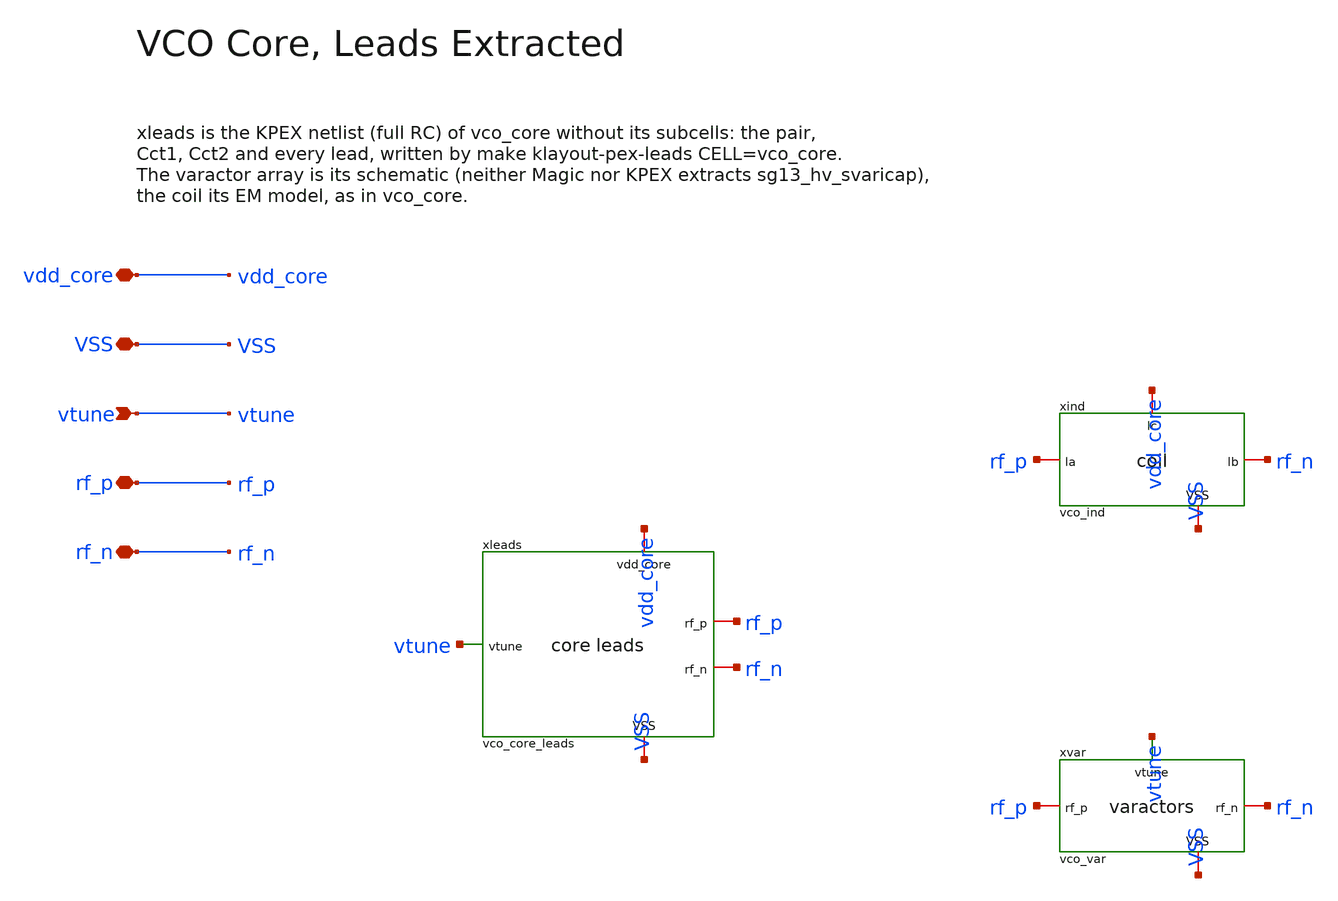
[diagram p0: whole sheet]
** sch_path: macros/vco/testbenches/xschem/vco_core_lpe.sch
**.subckt vco_core_lpe vdd_core VSS vtune rf_p rf_n
*.iopin vdd_core
*.iopin VSS
*.ipin vtune
*.iopin rf_p
*.iopin rf_n
xleads vdd_core VSS vtune rf_p rf_n vco_core_leads
xind rf_p rf_n vdd_core VSS vco_ind
xvar rf_p rf_n vtune VSS vco_var
**.ends

* expanding   symbol:  vco_ind.sym # of pins=4
** sym_path: macros/vco/schematic/xschem/vco_ind.sym
** sch_path: macros/vco/schematic/xschem/vco_ind.sch
.subckt vco_ind la lb lc VSS
*.iopin la
*.iopin lc
*.iopin lb
*.iopin VSS
XL1 la lc lb VSS inductor3 w=4e-6 s=4e-6 d=52e-6 nr_r=2 m=1
x1 la lb lc vco_ind_le
.ends


* expanding   symbol:  vco_var.sym # of pins=4
** sym_path: macros/vco/schematic/xschem/vco_var.sym
** sch_path: macros/vco/schematic/xschem/vco_var.sch
.subckt vco_var rf_p rf_n vtune VSS
*.ipin vtune
*.iopin rf_p
*.iopin rf_n
*.iopin VSS
XCvar1 rf_p vtune rf_n VSS sg13_hv_svaricap w=3.74u l=0.3u Nx=7 mm_ok=1
XCvar2 rf_p vtune rf_n VSS sg13_hv_svaricap w=3.74u l=0.3u Nx=7 mm_ok=1
XCvar3 rf_p vtune rf_n VSS sg13_hv_svaricap w=3.74u l=0.3u Nx=7 mm_ok=1
.ends

.end
